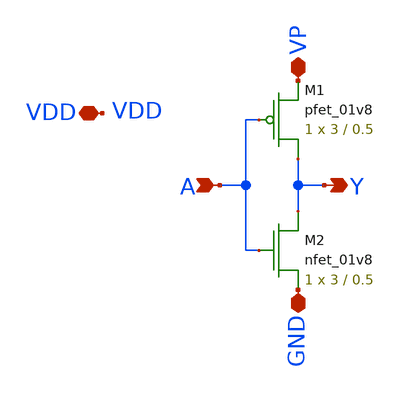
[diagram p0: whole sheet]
** sch_path: final/LDS/inverter.sch
**.subckt inverter A VP GND Y VDD
*.ipin A
*.iopin VP
*.iopin GND
*.opin Y
*.iopin VDD
XM1 Y A VP VDD sky130_fd_pr__pfet_01v8 L=0.5 W=3 nf=1 ad='int((nf+1)/2) * W/nf * 0.29' as='int((nf+2)/2) * W/nf * 0.29'
+ pd='2*int((nf+1)/2) * (W/nf + 0.29)' ps='2*int((nf+2)/2) * (W/nf + 0.29)' nrd='0.29 / W' nrs='0.29 / W'
+ sa=0 sb=0 sd=0 mult=1 m=1
XM2 Y A GND GND sky130_fd_pr__nfet_01v8 L=0.5 W=3 nf=1 ad='int((nf+1)/2) * W/nf * 0.29' as='int((nf+2)/2) * W/nf * 0.29'
+ pd='2*int((nf+1)/2) * (W/nf + 0.29)' ps='2*int((nf+2)/2) * (W/nf + 0.29)' nrd='0.29 / W' nrs='0.29 / W'
+ sa=0 sb=0 sd=0 mult=1 m=1
**.ends
.end
